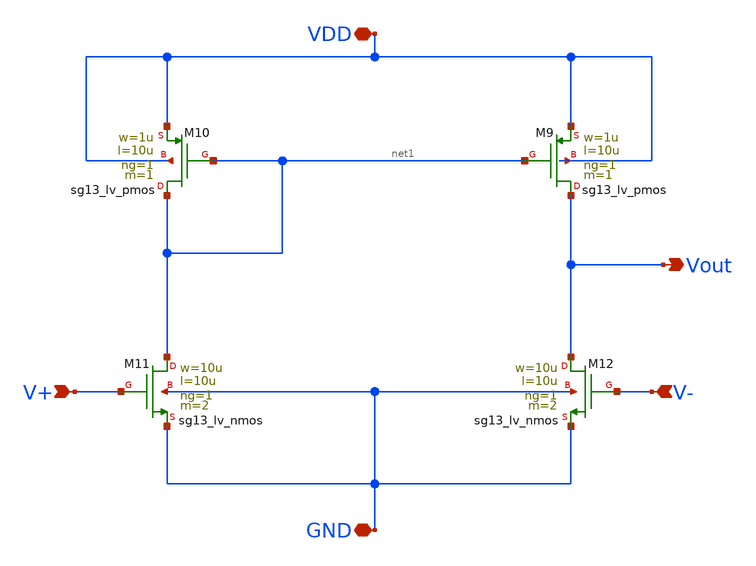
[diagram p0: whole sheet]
** sch_path: SSDOR_1V_v1/components/Ib_4u/Ib_4u_opamp/Ib_4u_opamp.sch
**.subckt Ib_4u_opamp VDD V+ V- Vout GND
*.iopin VDD
*.ipin V+
*.ipin V-
*.opin Vout
*.iopin GND
XM9 Vout net1 VDD VDD sg13_lv_pmos w=1u l=10u ng=1 m=1 mm_ok=1
XM10 net1 net1 VDD VDD sg13_lv_pmos w=1u l=10u ng=1 m=1 mm_ok=1
XM11 net1 V+ GND GND sg13_lv_nmos w=10u l=10u ng=1 m=2 mm_ok=1
XM12 Vout V- GND GND sg13_lv_nmos w=10u l=10u ng=1 m=2 mm_ok=1
**.ends
.end
